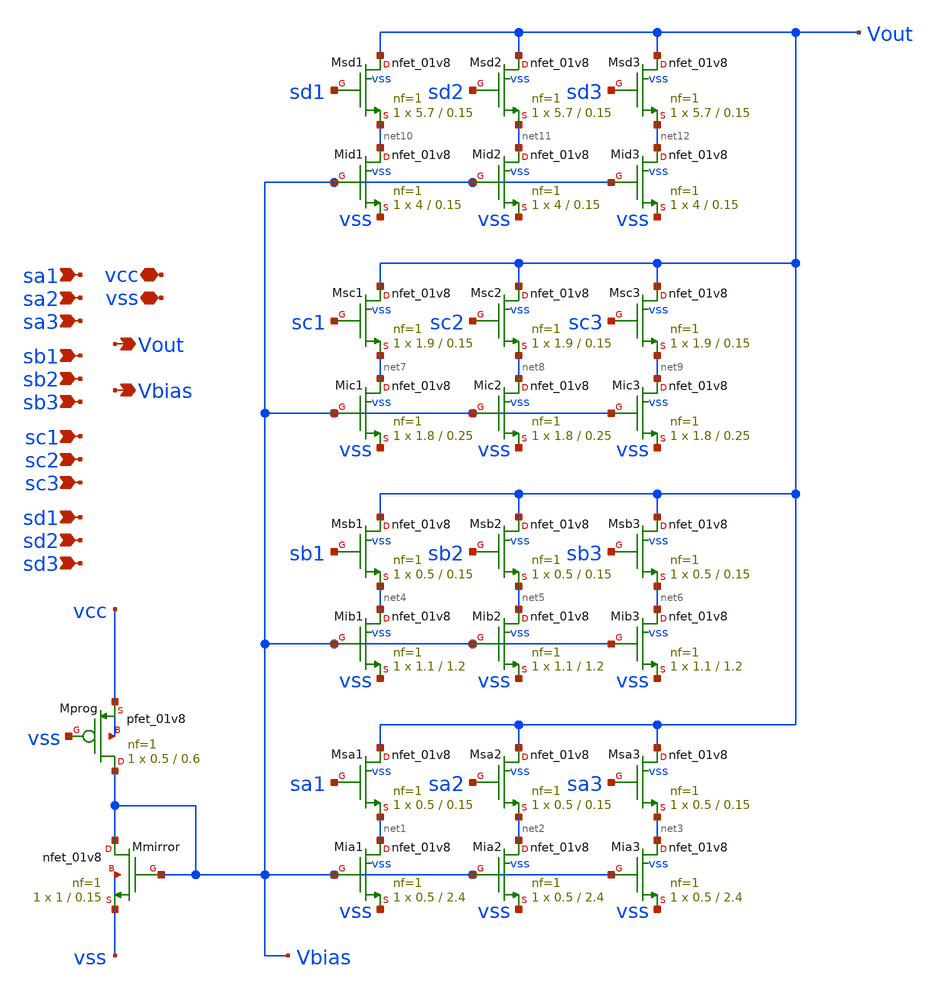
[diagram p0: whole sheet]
** sch_path: xschem/segdac.sch
**.subckt segdac vcc vss Vout Vbias sa1 sa2 sa3 sb1 sb2 sb3 sc1 sc2 sc3 sd1 sd2 sd3
*.iopin vcc
*.iopin vss
*.opin Vout
*.opin Vbias
*.ipin sa1
*.ipin sa2
*.ipin sa3
*.ipin sb1
*.ipin sb2
*.ipin sb3
*.ipin sc1
*.ipin sc2
*.ipin sc3
*.ipin sd1
*.ipin sd2
*.ipin sd3
XMprog Vbias vss vcc vcc sky130_fd_pr__pfet_01v8 L=0.6 W=0.5 nf=1 ad='int((nf+1)/2) * W/nf * 0.29' as='int((nf+2)/2) * W/nf * 0.29'
+ pd='2*int((nf+1)/2) * (W/nf + 0.29)' ps='2*int((nf+2)/2) * (W/nf + 0.29)' nrd='0.29 / W' nrs='0.29 / W'
+ sa=0 sb=0 sd=0 mult=1 m=1
XMmirror Vbias Vbias vss vss sky130_fd_pr__nfet_01v8 L=0.15 W=1 nf=1 ad='int((nf+1)/2) * W/nf * 0.29'
+ as='int((nf+2)/2) * W/nf * 0.29' pd='2*int((nf+1)/2) * (W/nf + 0.29)' ps='2*int((nf+2)/2) * (W/nf + 0.29)'
+ nrd='0.29 / W' nrs='0.29 / W' sa=0 sb=0 sd=0 mult=1 m=1
XMia1 net1 Vbias vss vss sky130_fd_pr__nfet_01v8 L=2.4 W=0.5 nf=1 ad='int((nf+1)/2) * W/nf * 0.29' as='int((nf+2)/2) * W/nf * 0.29'
+ pd='2*int((nf+1)/2) * (W/nf + 0.29)' ps='2*int((nf+2)/2) * (W/nf + 0.29)' nrd='0.29 / W' nrs='0.29 / W'
+ sa=0 sb=0 sd=0 mult=1 m=1
XMia2 net2 Vbias vss vss sky130_fd_pr__nfet_01v8 L=2.4 W=0.5 nf=1 ad='int((nf+1)/2) * W/nf * 0.29' as='int((nf+2)/2) * W/nf * 0.29'
+ pd='2*int((nf+1)/2) * (W/nf + 0.29)' ps='2*int((nf+2)/2) * (W/nf + 0.29)' nrd='0.29 / W' nrs='0.29 / W'
+ sa=0 sb=0 sd=0 mult=1 m=1
XMia3 net3 Vbias vss vss sky130_fd_pr__nfet_01v8 L=2.4 W=0.5 nf=1 ad='int((nf+1)/2) * W/nf * 0.29' as='int((nf+2)/2) * W/nf * 0.29'
+ pd='2*int((nf+1)/2) * (W/nf + 0.29)' ps='2*int((nf+2)/2) * (W/nf + 0.29)' nrd='0.29 / W' nrs='0.29 / W'
+ sa=0 sb=0 sd=0 mult=1 m=1
XMsa1 Vout sa1 net1 vss sky130_fd_pr__nfet_01v8 L=0.15 W=0.5 nf=1 ad='int((nf+1)/2) * W/nf * 0.29' as='int((nf+2)/2) * W/nf * 0.29'
+ pd='2*int((nf+1)/2) * (W/nf + 0.29)' ps='2*int((nf+2)/2) * (W/nf + 0.29)' nrd='0.29 / W' nrs='0.29 / W'
+ sa=0 sb=0 sd=0 mult=1 m=1
XMsa2 Vout sa2 net2 vss sky130_fd_pr__nfet_01v8 L=0.15 W=0.5 nf=1 ad='int((nf+1)/2) * W/nf * 0.29' as='int((nf+2)/2) * W/nf * 0.29'
+ pd='2*int((nf+1)/2) * (W/nf + 0.29)' ps='2*int((nf+2)/2) * (W/nf + 0.29)' nrd='0.29 / W' nrs='0.29 / W'
+ sa=0 sb=0 sd=0 mult=1 m=1
XMsa3 Vout sa3 net3 vss sky130_fd_pr__nfet_01v8 L=0.15 W=0.5 nf=1 ad='int((nf+1)/2) * W/nf * 0.29' as='int((nf+2)/2) * W/nf * 0.29'
+ pd='2*int((nf+1)/2) * (W/nf + 0.29)' ps='2*int((nf+2)/2) * (W/nf + 0.29)' nrd='0.29 / W' nrs='0.29 / W'
+ sa=0 sb=0 sd=0 mult=1 m=1
XMib1 net4 Vbias vss vss sky130_fd_pr__nfet_01v8 L=1.2 W=1.1 nf=1 ad='int((nf+1)/2) * W/nf * 0.29' as='int((nf+2)/2) * W/nf * 0.29'
+ pd='2*int((nf+1)/2) * (W/nf + 0.29)' ps='2*int((nf+2)/2) * (W/nf + 0.29)' nrd='0.29 / W' nrs='0.29 / W'
+ sa=0 sb=0 sd=0 mult=1 m=1
XMib2 net5 Vbias vss vss sky130_fd_pr__nfet_01v8 L=1.2 W=1.1 nf=1 ad='int((nf+1)/2) * W/nf * 0.29' as='int((nf+2)/2) * W/nf * 0.29'
+ pd='2*int((nf+1)/2) * (W/nf + 0.29)' ps='2*int((nf+2)/2) * (W/nf + 0.29)' nrd='0.29 / W' nrs='0.29 / W'
+ sa=0 sb=0 sd=0 mult=1 m=1
XMib3 net6 Vbias vss vss sky130_fd_pr__nfet_01v8 L=1.2 W=1.1 nf=1 ad='int((nf+1)/2) * W/nf * 0.29' as='int((nf+2)/2) * W/nf * 0.29'
+ pd='2*int((nf+1)/2) * (W/nf + 0.29)' ps='2*int((nf+2)/2) * (W/nf + 0.29)' nrd='0.29 / W' nrs='0.29 / W'
+ sa=0 sb=0 sd=0 mult=1 m=1
XMsb1 Vout sb1 net4 vss sky130_fd_pr__nfet_01v8 L=0.15 W=0.5 nf=1 ad='int((nf+1)/2) * W/nf * 0.29' as='int((nf+2)/2) * W/nf * 0.29'
+ pd='2*int((nf+1)/2) * (W/nf + 0.29)' ps='2*int((nf+2)/2) * (W/nf + 0.29)' nrd='0.29 / W' nrs='0.29 / W'
+ sa=0 sb=0 sd=0 mult=1 m=1
XMsb2 Vout sb2 net5 vss sky130_fd_pr__nfet_01v8 L=0.15 W=0.5 nf=1 ad='int((nf+1)/2) * W/nf * 0.29' as='int((nf+2)/2) * W/nf * 0.29'
+ pd='2*int((nf+1)/2) * (W/nf + 0.29)' ps='2*int((nf+2)/2) * (W/nf + 0.29)' nrd='0.29 / W' nrs='0.29 / W'
+ sa=0 sb=0 sd=0 mult=1 m=1
XMsb3 Vout sb3 net6 vss sky130_fd_pr__nfet_01v8 L=0.15 W=0.5 nf=1 ad='int((nf+1)/2) * W/nf * 0.29' as='int((nf+2)/2) * W/nf * 0.29'
+ pd='2*int((nf+1)/2) * (W/nf + 0.29)' ps='2*int((nf+2)/2) * (W/nf + 0.29)' nrd='0.29 / W' nrs='0.29 / W'
+ sa=0 sb=0 sd=0 mult=1 m=1
XMic1 net7 Vbias vss vss sky130_fd_pr__nfet_01v8 L=0.25 W=1.8 nf=1 ad='int((nf+1)/2) * W/nf * 0.29' as='int((nf+2)/2) * W/nf * 0.29'
+ pd='2*int((nf+1)/2) * (W/nf + 0.29)' ps='2*int((nf+2)/2) * (W/nf + 0.29)' nrd='0.29 / W' nrs='0.29 / W'
+ sa=0 sb=0 sd=0 mult=1 m=1
XMic2 net8 Vbias vss vss sky130_fd_pr__nfet_01v8 L=0.25 W=1.8 nf=1 ad='int((nf+1)/2) * W/nf * 0.29' as='int((nf+2)/2) * W/nf * 0.29'
+ pd='2*int((nf+1)/2) * (W/nf + 0.29)' ps='2*int((nf+2)/2) * (W/nf + 0.29)' nrd='0.29 / W' nrs='0.29 / W'
+ sa=0 sb=0 sd=0 mult=1 m=1
XMic3 net9 Vbias vss vss sky130_fd_pr__nfet_01v8 L=0.25 W=1.8 nf=1 ad='int((nf+1)/2) * W/nf * 0.29' as='int((nf+2)/2) * W/nf * 0.29'
+ pd='2*int((nf+1)/2) * (W/nf + 0.29)' ps='2*int((nf+2)/2) * (W/nf + 0.29)' nrd='0.29 / W' nrs='0.29 / W'
+ sa=0 sb=0 sd=0 mult=1 m=1
XMsc1 Vout sc1 net7 vss sky130_fd_pr__nfet_01v8 L=0.15 W=1.9 nf=1 ad='int((nf+1)/2) * W/nf * 0.29' as='int((nf+2)/2) * W/nf * 0.29'
+ pd='2*int((nf+1)/2) * (W/nf + 0.29)' ps='2*int((nf+2)/2) * (W/nf + 0.29)' nrd='0.29 / W' nrs='0.29 / W'
+ sa=0 sb=0 sd=0 mult=1 m=1
XMsc2 Vout sc2 net8 vss sky130_fd_pr__nfet_01v8 L=0.15 W=1.9 nf=1 ad='int((nf+1)/2) * W/nf * 0.29' as='int((nf+2)/2) * W/nf * 0.29'
+ pd='2*int((nf+1)/2) * (W/nf + 0.29)' ps='2*int((nf+2)/2) * (W/nf + 0.29)' nrd='0.29 / W' nrs='0.29 / W'
+ sa=0 sb=0 sd=0 mult=1 m=1
XMsc3 Vout sc3 net9 vss sky130_fd_pr__nfet_01v8 L=0.15 W=1.9 nf=1 ad='int((nf+1)/2) * W/nf * 0.29' as='int((nf+2)/2) * W/nf * 0.29'
+ pd='2*int((nf+1)/2) * (W/nf + 0.29)' ps='2*int((nf+2)/2) * (W/nf + 0.29)' nrd='0.29 / W' nrs='0.29 / W'
+ sa=0 sb=0 sd=0 mult=1 m=1
XMid1 net10 Vbias vss vss sky130_fd_pr__nfet_01v8 L=0.15 W=4 nf=1 ad='int((nf+1)/2) * W/nf * 0.29' as='int((nf+2)/2) * W/nf * 0.29'
+ pd='2*int((nf+1)/2) * (W/nf + 0.29)' ps='2*int((nf+2)/2) * (W/nf + 0.29)' nrd='0.29 / W' nrs='0.29 / W'
+ sa=0 sb=0 sd=0 mult=1 m=1
XMid2 net11 Vbias vss vss sky130_fd_pr__nfet_01v8 L=0.15 W=4 nf=1 ad='int((nf+1)/2) * W/nf * 0.29' as='int((nf+2)/2) * W/nf * 0.29'
+ pd='2*int((nf+1)/2) * (W/nf + 0.29)' ps='2*int((nf+2)/2) * (W/nf + 0.29)' nrd='0.29 / W' nrs='0.29 / W'
+ sa=0 sb=0 sd=0 mult=1 m=1
XMid3 net12 Vbias vss vss sky130_fd_pr__nfet_01v8 L=0.15 W=4 nf=1 ad='int((nf+1)/2) * W/nf * 0.29' as='int((nf+2)/2) * W/nf * 0.29'
+ pd='2*int((nf+1)/2) * (W/nf + 0.29)' ps='2*int((nf+2)/2) * (W/nf + 0.29)' nrd='0.29 / W' nrs='0.29 / W'
+ sa=0 sb=0 sd=0 mult=1 m=1
XMsd1 Vout sd1 net10 vss sky130_fd_pr__nfet_01v8 L=0.15 W=5.7 nf=1 ad='int((nf+1)/2) * W/nf * 0.29' as='int((nf+2)/2) * W/nf * 0.29'
+ pd='2*int((nf+1)/2) * (W/nf + 0.29)' ps='2*int((nf+2)/2) * (W/nf + 0.29)' nrd='0.29 / W' nrs='0.29 / W'
+ sa=0 sb=0 sd=0 mult=1 m=1
XMsd2 Vout sd2 net11 vss sky130_fd_pr__nfet_01v8 L=0.15 W=5.7 nf=1 ad='int((nf+1)/2) * W/nf * 0.29' as='int((nf+2)/2) * W/nf * 0.29'
+ pd='2*int((nf+1)/2) * (W/nf + 0.29)' ps='2*int((nf+2)/2) * (W/nf + 0.29)' nrd='0.29 / W' nrs='0.29 / W'
+ sa=0 sb=0 sd=0 mult=1 m=1
XMsd3 Vout sd3 net12 vss sky130_fd_pr__nfet_01v8 L=0.15 W=5.7 nf=1 ad='int((nf+1)/2) * W/nf * 0.29' as='int((nf+2)/2) * W/nf * 0.29'
+ pd='2*int((nf+1)/2) * (W/nf + 0.29)' ps='2*int((nf+2)/2) * (W/nf + 0.29)' nrd='0.29 / W' nrs='0.29 / W'
+ sa=0 sb=0 sd=0 mult=1 m=1
**.ends
.end
